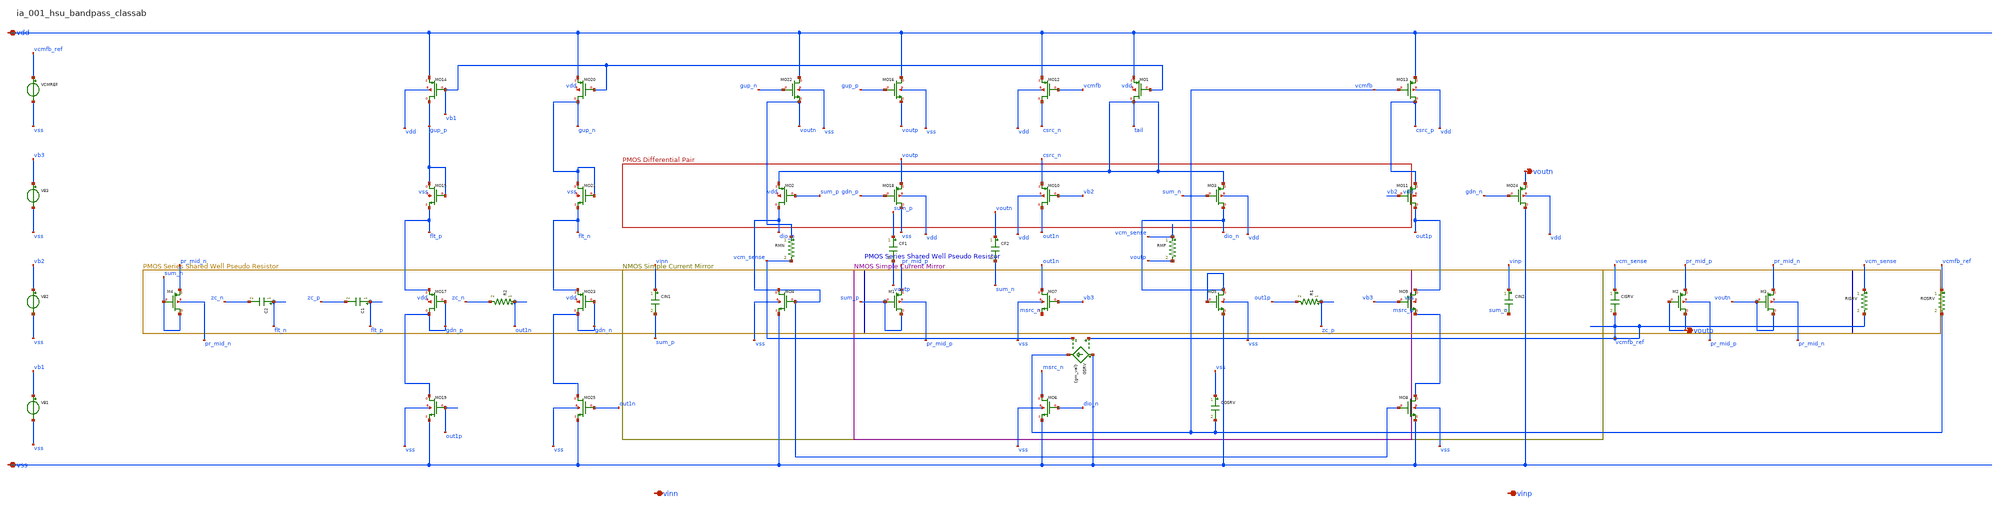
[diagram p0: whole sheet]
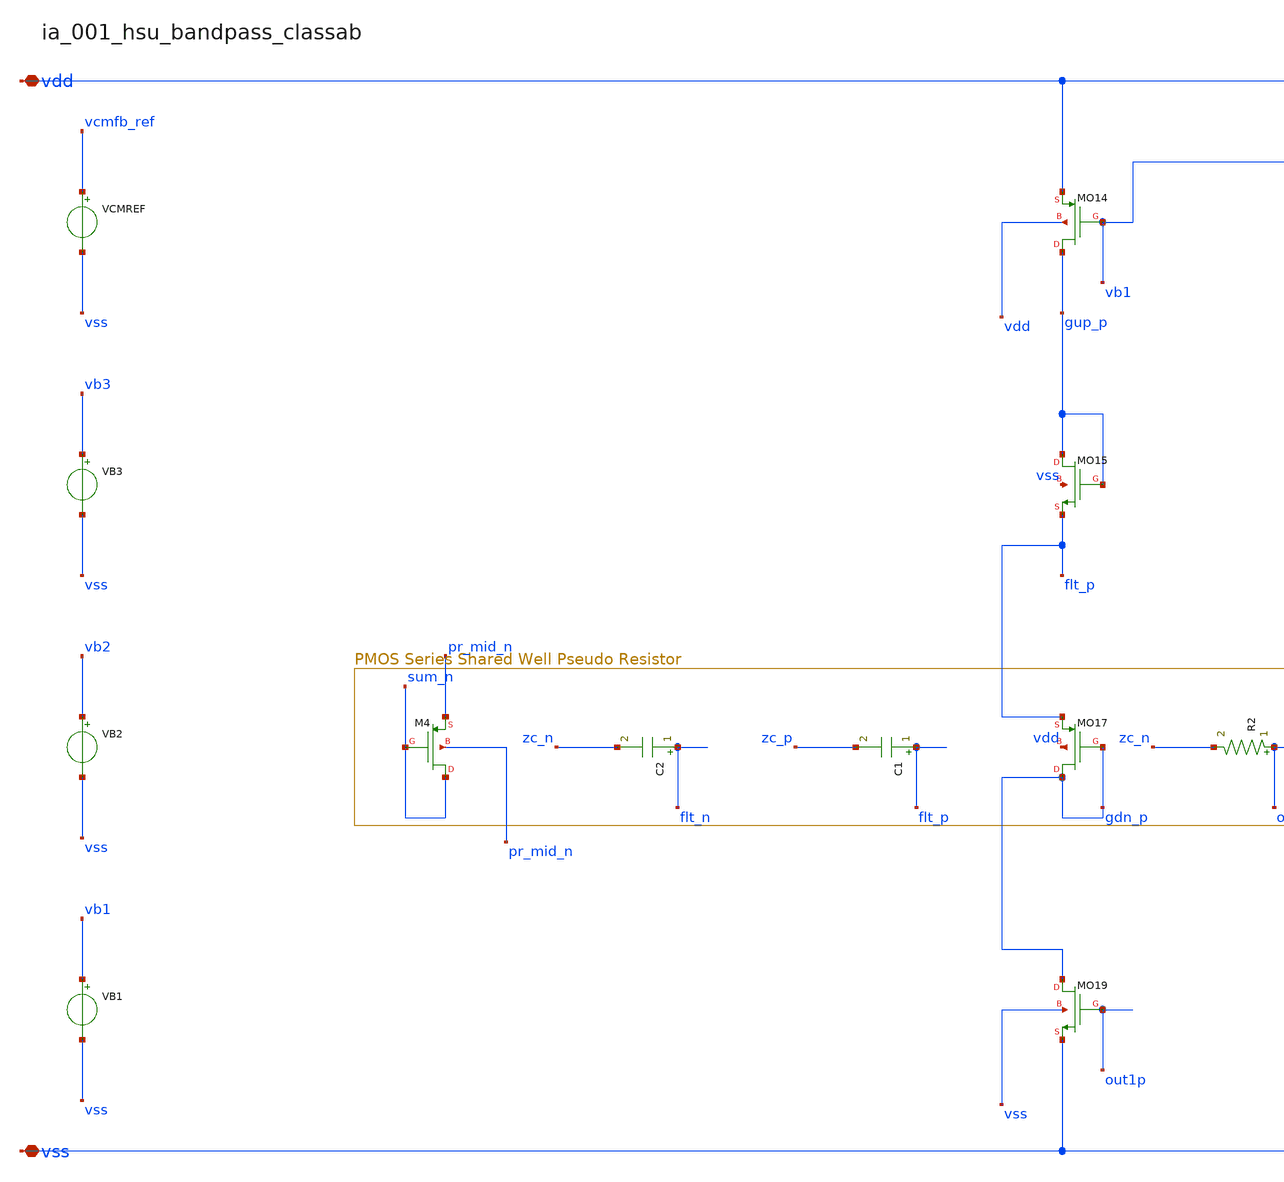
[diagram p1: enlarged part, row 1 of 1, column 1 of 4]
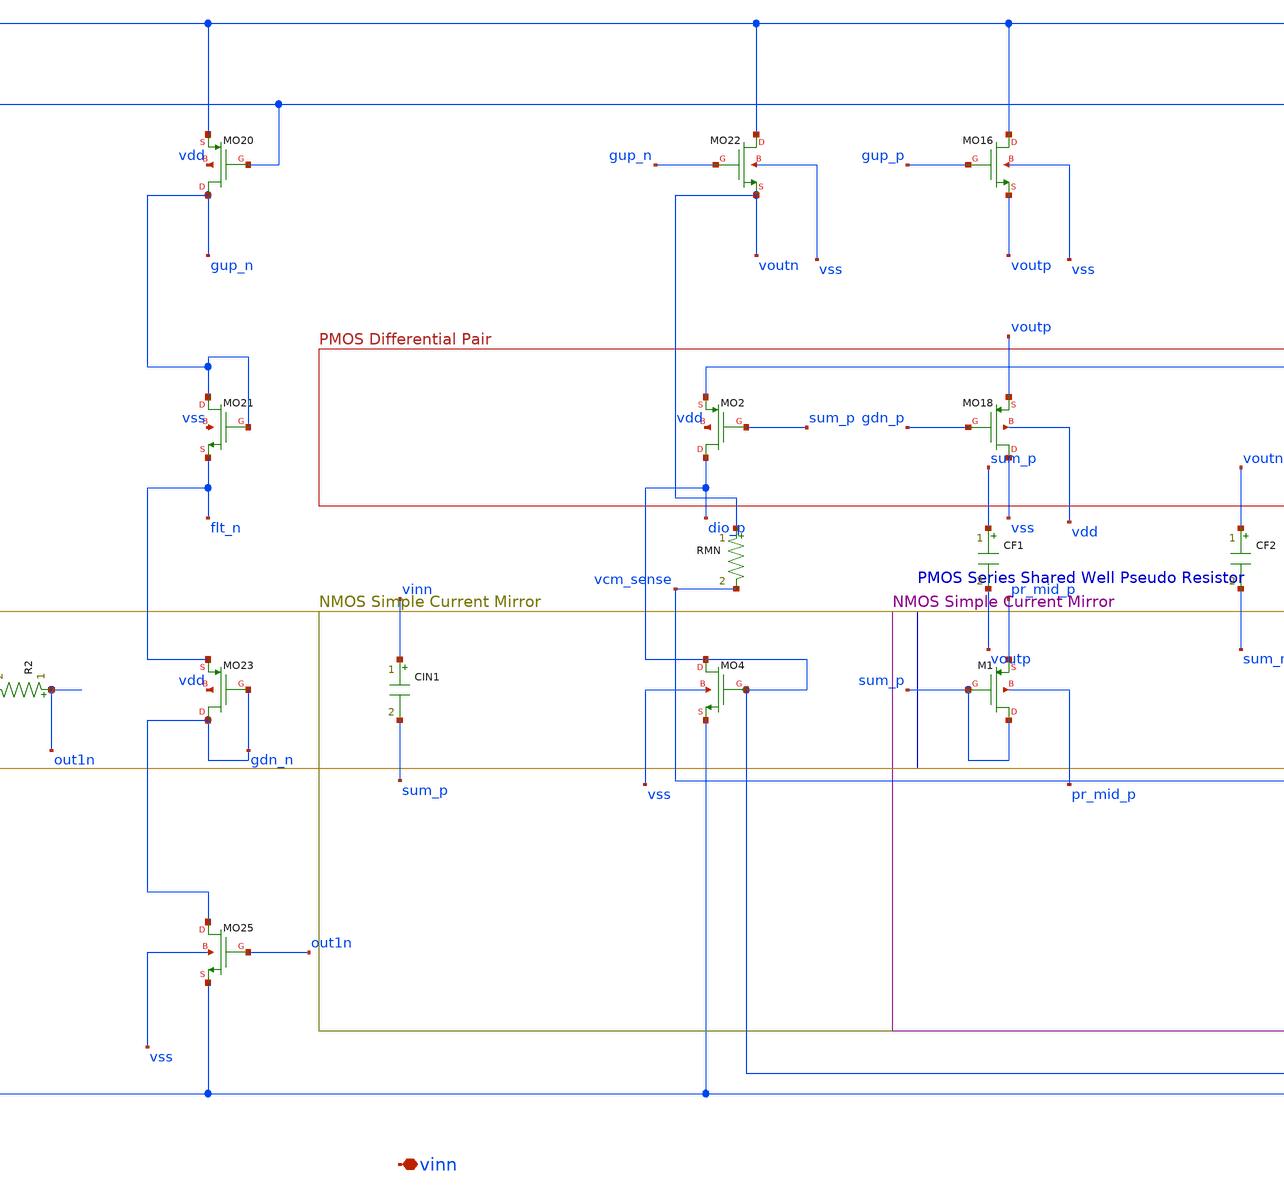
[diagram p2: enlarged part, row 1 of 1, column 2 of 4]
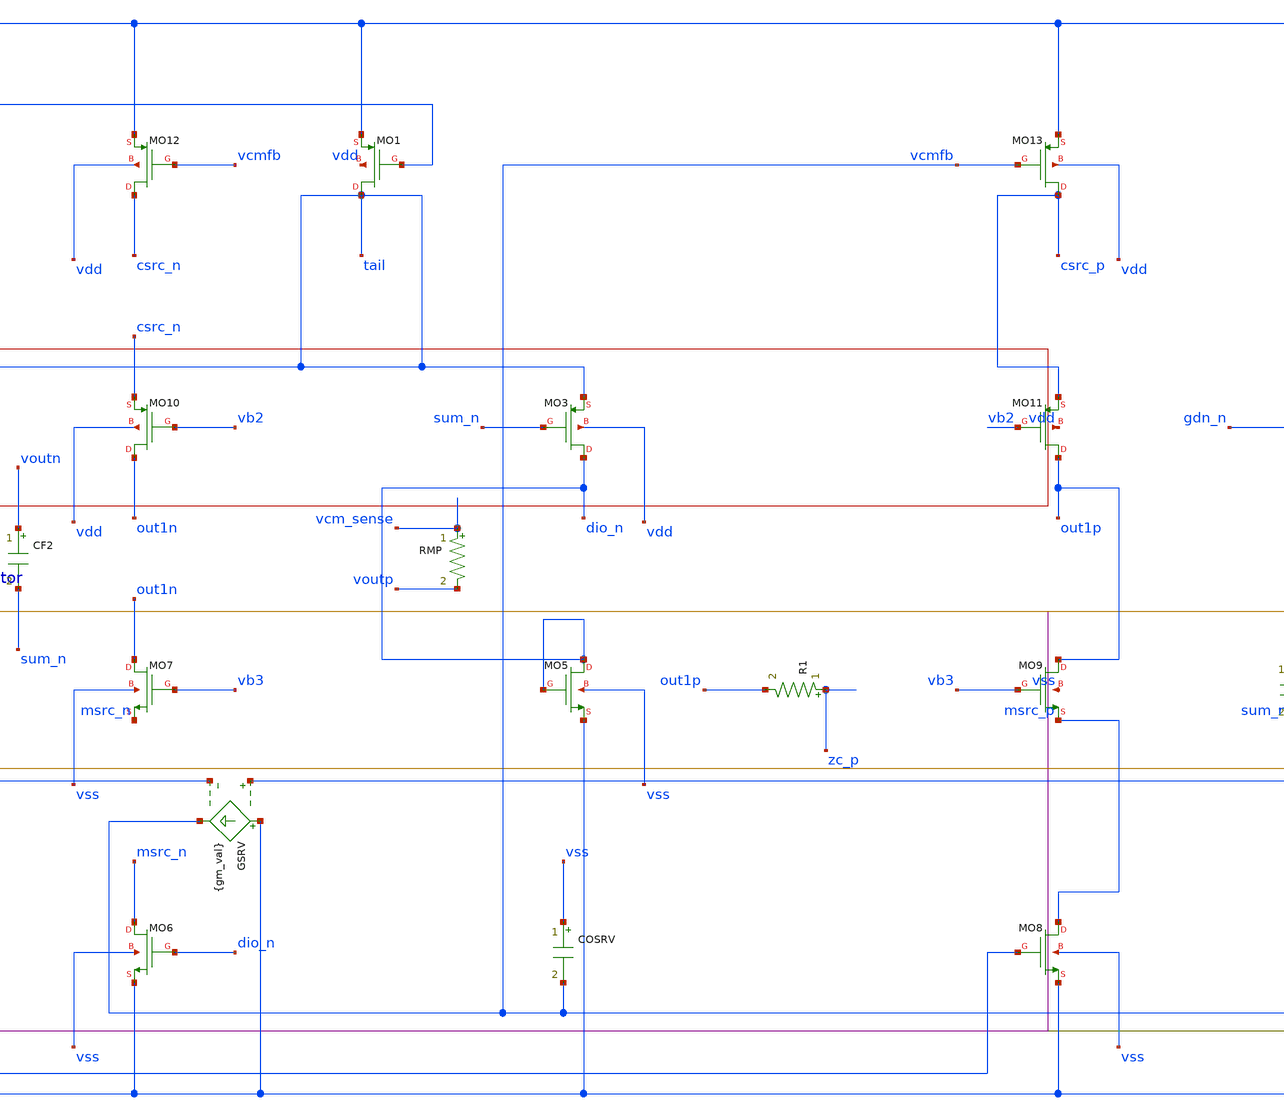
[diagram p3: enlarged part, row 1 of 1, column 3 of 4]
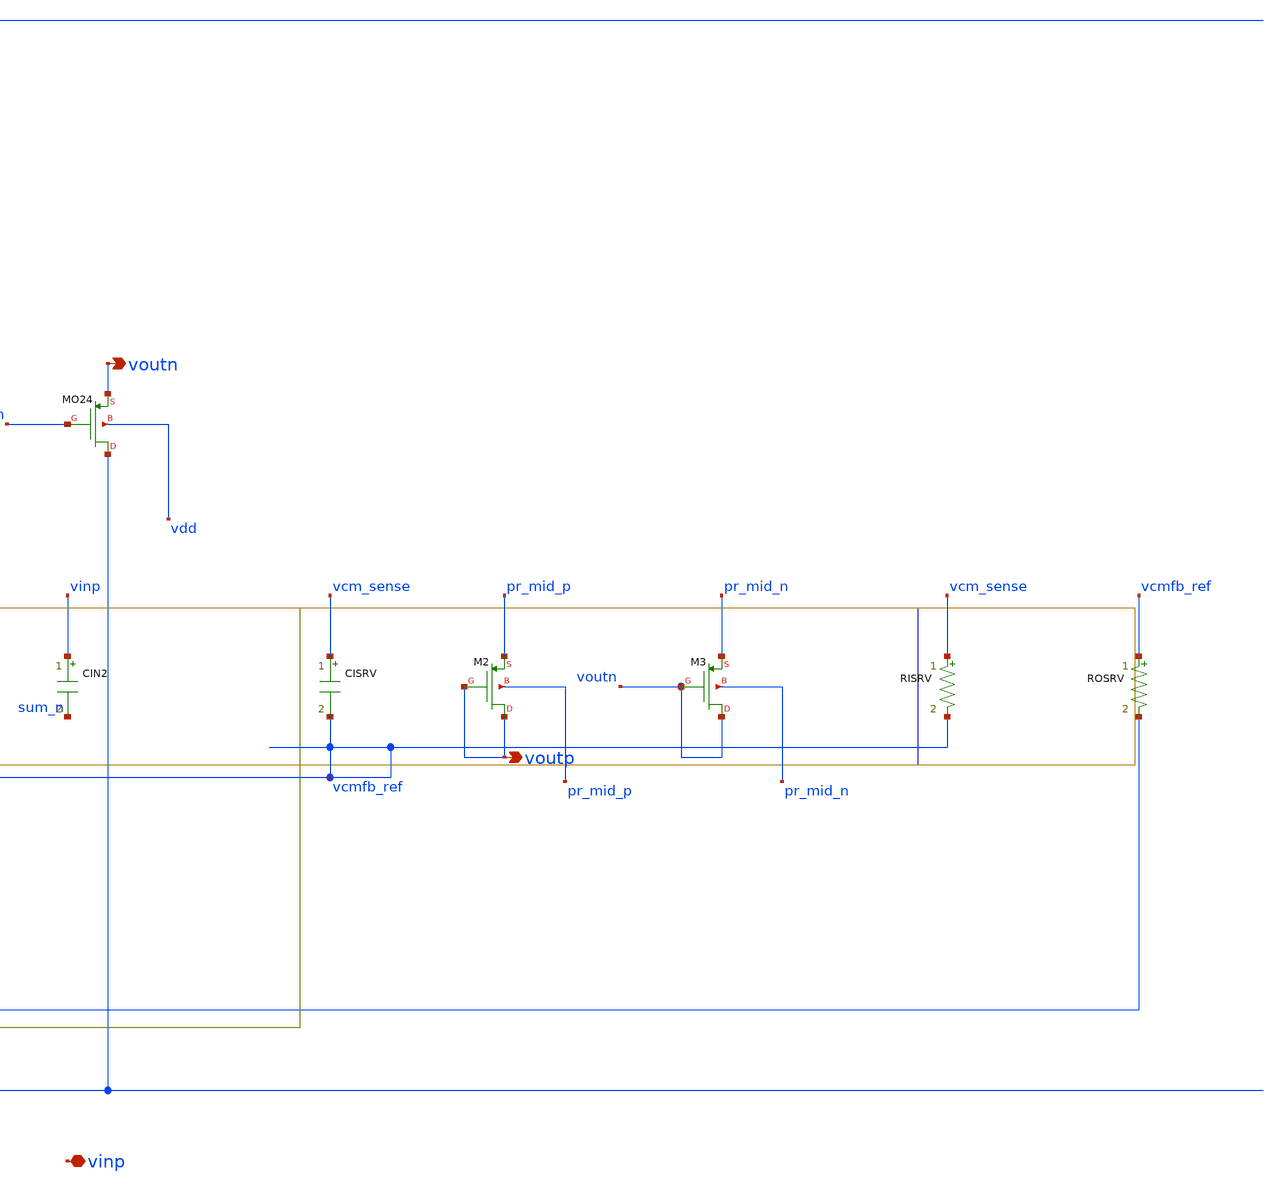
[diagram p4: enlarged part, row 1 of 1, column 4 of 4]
** sch_path: analog-db/raw/ia_001_hsu_bandpass_classab/ia_001_hsu_bandpass_classab_annotated.sch
**.subckt ia_001_hsu_bandpass_classab_annotated vdd vss voutn voutp vinn vinp
*.iopin vdd
*.iopin vss
*.opin voutn
*.opin voutp
*.iopin vinn
*.iopin vinp
C1 flt_p zc_p 'x_dut_c1_value' m=1
C2 flt_n zc_n 'x_dut_c2_value' m=1
CF1 sum_p voutp 'x_dut_cf1_value' m=1
CF2 voutn sum_n 'x_dut_cf2_value' m=1
CIN1 vinn sum_p 'x_dut_cin1_value' m=1
CIN2 vinp sum_n 'x_dut_cin2_value' m=1
CISRV vcm_sense vcmfb_ref 'cin_val' m=1
COSRV vss vcmfb 'cout_val' m=1
GSRV vss vcmfb vcmfb_ref vcm_sense {gm_val}
R1 zc_p out1p 'x_dut_r1_value' m=1
R2 out1n zc_n 'x_dut_r2_value' m=1
RISRV vcm_sense vcmfb_ref 'rin_val' m=1
RMN voutn vcm_sense 'x_dut_rmn_value' m=1
RMP vcm_sense voutp 'x_dut_rmp_value' m=1
ROSRV vcmfb_ref vcmfb 'rout_val' m=1
VB1 vb1 vss dc {vb1}
VB2 vb2 vss dc {vb2}
VB3 vb3 vss dc {vb3}
VCMREF vcmfb_ref vss dc {vcmfb_ref}
XM1 sum_p sum_p pr_mid_p pr_mid_p sg13_lv_pmos w=x_dut_xm1_w l=x_dut_xm1_l ng=1 m=x_dut_xm1_m
XM2 voutp voutp pr_mid_p pr_mid_p sg13_lv_pmos w=x_dut_xm2_w l=x_dut_xm2_l ng=1 m=x_dut_xm2_m
XM3 voutn voutn pr_mid_n pr_mid_n sg13_lv_pmos w=x_dut_xm3_w l=x_dut_xm3_l ng=1 m=x_dut_xm3_m
XM4 sum_n sum_n pr_mid_n pr_mid_n sg13_lv_pmos w=x_dut_xm4_w l=x_dut_xm4_l ng=1 m=x_dut_xm4_m
XMO1 tail vb1 vdd vdd sg13_lv_pmos w=x_dut_xmo1_w l=x_dut_xmo1_l ng=1 m=x_dut_xmo1_m
XMO10 out1n vb2 csrc_n vdd sg13_lv_pmos w=x_dut_xmo10_w l=x_dut_xmo10_l ng=1 m=x_dut_xmo10_m
XMO11 out1p vb2 csrc_p vdd sg13_lv_pmos w=x_dut_xmo11_w l=x_dut_xmo11_l ng=1 m=x_dut_xmo11_m
XMO12 csrc_n vcmfb vdd vdd sg13_lv_pmos w=x_dut_xmo12_w l=x_dut_xmo12_l ng=1 m=x_dut_xmo12_m
XMO13 csrc_p vcmfb vdd vdd sg13_lv_pmos w=x_dut_xmo13_w l=x_dut_xmo13_l ng=1 m=x_dut_xmo13_m
XMO14 gup_p vb1 vdd vdd sg13_lv_pmos w=x_dut_xmo14_w l=x_dut_xmo14_l ng=1 m=x_dut_xmo14_m
XMO15 gup_p gup_p flt_p vss sg13_lv_nmos w=x_dut_xmo15_w l=x_dut_xmo15_l ng=1 m=x_dut_xmo15_m
XMO16 vdd gup_p voutp vss sg13_lv_nmos w=x_dut_xmo16_w l=x_dut_xmo16_l ng=1 m=x_dut_xmo16_m
XMO17 gdn_p gdn_p flt_p vdd sg13_lv_pmos w=x_dut_xmo17_w l=x_dut_xmo17_l ng=1 m=x_dut_xmo17_m
XMO18 vss gdn_p voutp vdd sg13_lv_pmos w=x_dut_xmo18_w l=x_dut_xmo18_l ng=1 m=x_dut_xmo18_m
XMO19 gdn_p out1p vss vss sg13_lv_nmos w=x_dut_xmo19_w l=x_dut_xmo19_l ng=1 m=x_dut_xmo19_m
XMO2 dio_p sum_p tail vdd sg13_lv_pmos w=x_dut_xmo2_w l=x_dut_xmo2_l ng=1 m=x_dut_xmo2_m
XMO20 gup_n vb1 vdd vdd sg13_lv_pmos w=x_dut_xmo20_w l=x_dut_xmo20_l ng=1 m=x_dut_xmo20_m
XMO21 gup_n gup_n flt_n vss sg13_lv_nmos w=x_dut_xmo21_w l=x_dut_xmo21_l ng=1 m=x_dut_xmo21_m
XMO22 vdd gup_n voutn vss sg13_lv_nmos w=x_dut_xmo22_w l=x_dut_xmo22_l ng=1 m=x_dut_xmo22_m
XMO23 gdn_n gdn_n flt_n vdd sg13_lv_pmos w=x_dut_xmo23_w l=x_dut_xmo23_l ng=1 m=x_dut_xmo23_m
XMO24 vss gdn_n voutn vdd sg13_lv_pmos w=x_dut_xmo24_w l=x_dut_xmo24_l ng=1 m=x_dut_xmo24_m
XMO25 gdn_n out1n vss vss sg13_lv_nmos w=x_dut_xmo25_w l=x_dut_xmo25_l ng=1 m=x_dut_xmo25_m
XMO3 dio_n sum_n tail vdd sg13_lv_pmos w=x_dut_xmo3_w l=x_dut_xmo3_l ng=1 m=x_dut_xmo3_m
XMO4 dio_p dio_p vss vss sg13_lv_nmos w=x_dut_xmo4_w l=x_dut_xmo4_l ng=1 m=x_dut_xmo4_m
XMO5 dio_n dio_n vss vss sg13_lv_nmos w=x_dut_xmo5_w l=x_dut_xmo5_l ng=1 m=x_dut_xmo5_m
XMO6 msrc_n dio_n vss vss sg13_lv_nmos w=x_dut_xmo6_w l=x_dut_xmo6_l ng=1 m=x_dut_xmo6_m
XMO7 out1n vb3 msrc_n vss sg13_lv_nmos w=x_dut_xmo7_w l=x_dut_xmo7_l ng=1 m=x_dut_xmo7_m
XMO8 msrc_p dio_p vss vss sg13_lv_nmos w=x_dut_xmo8_w l=x_dut_xmo8_l ng=1 m=x_dut_xmo8_m
XMO9 out1p vb3 msrc_p vss sg13_lv_nmos w=x_dut_xmo9_w l=x_dut_xmo9_l ng=1 m=x_dut_xmo9_m
**.ends
.end
